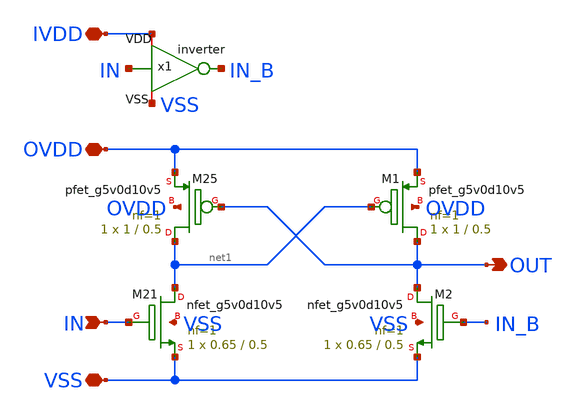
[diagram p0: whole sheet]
** sch_path: xschem/level_shifter.sch
**.subckt level_shifter OVDD VSS IN OUT IVDD
*.iopin OVDD
*.iopin VSS
*.ipin IN
*.opin OUT
*.iopin IVDD
XM21 net1 IN VSS VSS sky130_fd_pr__nfet_g5v0d10v5 L=0.5 W=0.65 nf=1 ad='int((1 + 1)/2) * 0.65 / 1 * 0.29'
+ as='int((1 + 2)/2) * 0.65 / 1 * 0.29' pd='2*int((1 + 1)/2) * (0.65 / 1 + 0.29)' ps='2*int((1 + 2)/2) * (0.65 / 1 + 0.29)'
+ nrd='0.29 / 0.65 ' nrs='0.29 / 0.65 ' sa=0 sb=0 sd=0 mult=1 m=1
XM25 net1 OUT OVDD OVDD sky130_fd_pr__pfet_g5v0d10v5 L=0.5 W=1 nf=1 ad='int((1 + 1)/2) * 1 / 1 * 0.29'
+ as='int((1 + 2)/2) * 1 / 1 * 0.29' pd='2*int((1 + 1)/2) * (1 / 1 + 0.29)' ps='2*int((1 + 2)/2) * (1 / 1 + 0.29)'
+ nrd='0.29 / 1 ' nrs='0.29 / 1 ' sa=0 sb=0 sd=0 mult=1 m=1
XM1 OUT net1 OVDD OVDD sky130_fd_pr__pfet_g5v0d10v5 L=0.5 W=1 nf=1 ad='int((1 + 1)/2) * 1 / 1 * 0.29'
+ as='int((1 + 2)/2) * 1 / 1 * 0.29' pd='2*int((1 + 1)/2) * (1 / 1 + 0.29)' ps='2*int((1 + 2)/2) * (1 / 1 + 0.29)'
+ nrd='0.29 / 1 ' nrs='0.29 / 1 ' sa=0 sb=0 sd=0 mult=1 m=1
XM2 OUT IN_B VSS VSS sky130_fd_pr__nfet_g5v0d10v5 L=0.5 W=0.65 nf=1 ad='int((1 + 1)/2) * 0.65 / 1 * 0.29'
+ as='int((1 + 2)/2) * 0.65 / 1 * 0.29' pd='2*int((1 + 1)/2) * (0.65 / 1 + 0.29)' ps='2*int((1 + 2)/2) * (0.65 / 1 + 0.29)'
+ nrd='0.29 / 0.65 ' nrs='0.29 / 0.65 ' sa=0 sb=0 sd=0 mult=1 m=1
x1 IVDD IN IN_B VSS inverter
**.ends

* expanding   symbol:  inverter.sym # of pins=4
** sym_path: xschem/inverter.sym
** sch_path: xschem/inverter.sch
.subckt inverter VDD IN OUT VSS
*.iopin VSS
*.iopin VDD
*.ipin IN
*.opin OUT
XM1 OUT IN VSS VSS sky130_fd_pr__nfet_g5v0d10v5 L=0.5 W=0.65 nf=1 ad='int((1 + 1)/2) * 0.65 / 1 * 0.29'
+ as='int((1 + 2)/2) * 0.65 / 1 * 0.29' pd='2*int((1 + 1)/2) * (0.65 / 1 + 0.29)' ps='2*int((1 + 2)/2) * (0.65 / 1 + 0.29)'
+ nrd='0.29 / 0.65 ' nrs='0.29 / 0.65 ' sa=0 sb=0 sd=0 mult=1 m=1
XM2 OUT IN VDD VDD sky130_fd_pr__pfet_g5v0d10v5 L=0.5 W=1 nf=1 ad='int((1 + 1)/2) * 1 / 1 * 0.29' as='int((1 + 2)/2) * 1 / 1 * 0.29'
+ pd='2*int((1 + 1)/2) * (1 / 1 + 0.29)' ps='2*int((1 + 2)/2) * (1 / 1 + 0.29)' nrd='0.29 / 1 ' nrs='0.29 / 1 '
+ sa=0 sb=0 sd=0 mult=1 m=1
.ends

.end
